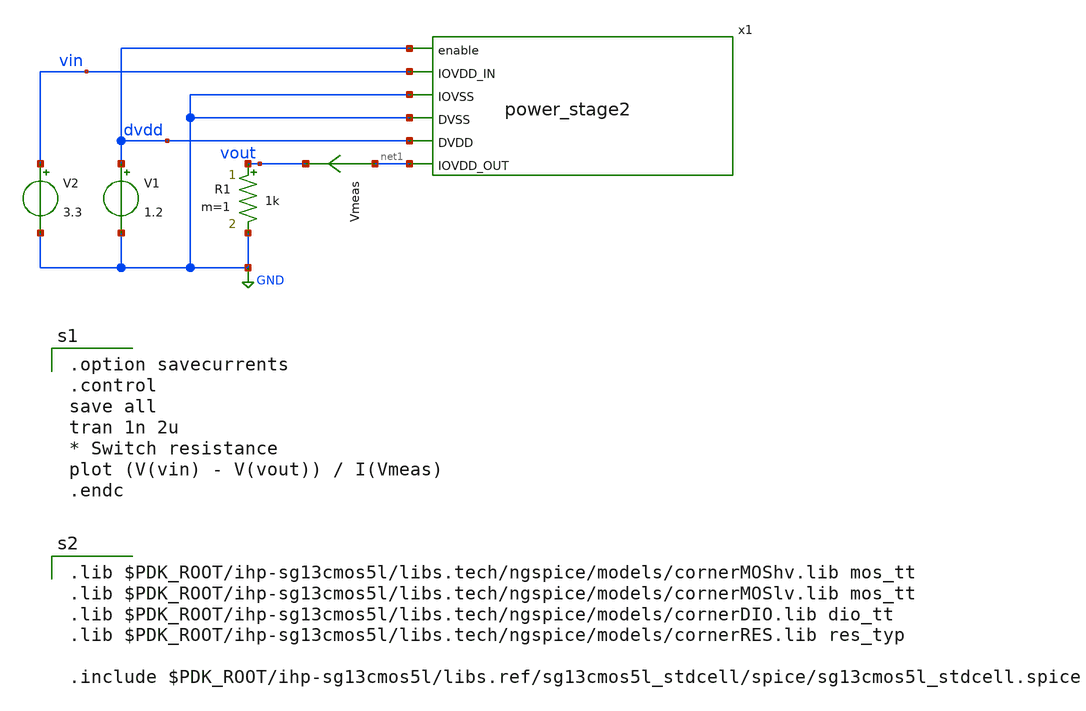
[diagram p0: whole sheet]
** sch_path: xschem/power_stage2_tb.sch
**.subckt power_stage2_tb
x1 dvdd vin GND GND dvdd net1 power_stage2
Vmeas net1 vout 0
.save i(vmeas)
R1 vout GND 1k m=1
V1 dvdd GND 1.2
V2 vin GND 3.3
**** begin user architecture code

.option savecurrents
.control
save all
tran 1n 2u
* Switch resistance
plot (V(vin) - V(vout)) / I(Vmeas)
.endc


.lib $PDK_ROOT/ihp-sg13cmos5l/libs.tech/ngspice/models/cornerMOShv.lib mos_tt
.lib $PDK_ROOT/ihp-sg13cmos5l/libs.tech/ngspice/models/cornerMOSlv.lib mos_tt
.lib $PDK_ROOT/ihp-sg13cmos5l/libs.tech/ngspice/models/cornerDIO.lib dio_tt
.lib $PDK_ROOT/ihp-sg13cmos5l/libs.tech/ngspice/models/cornerRES.lib res_typ

.include $PDK_ROOT/ihp-sg13cmos5l/libs.ref/sg13cmos5l_stdcell/spice/sg13cmos5l_stdcell.spice

**** end user architecture code
**.ends
.GLOBAL GND
.end
